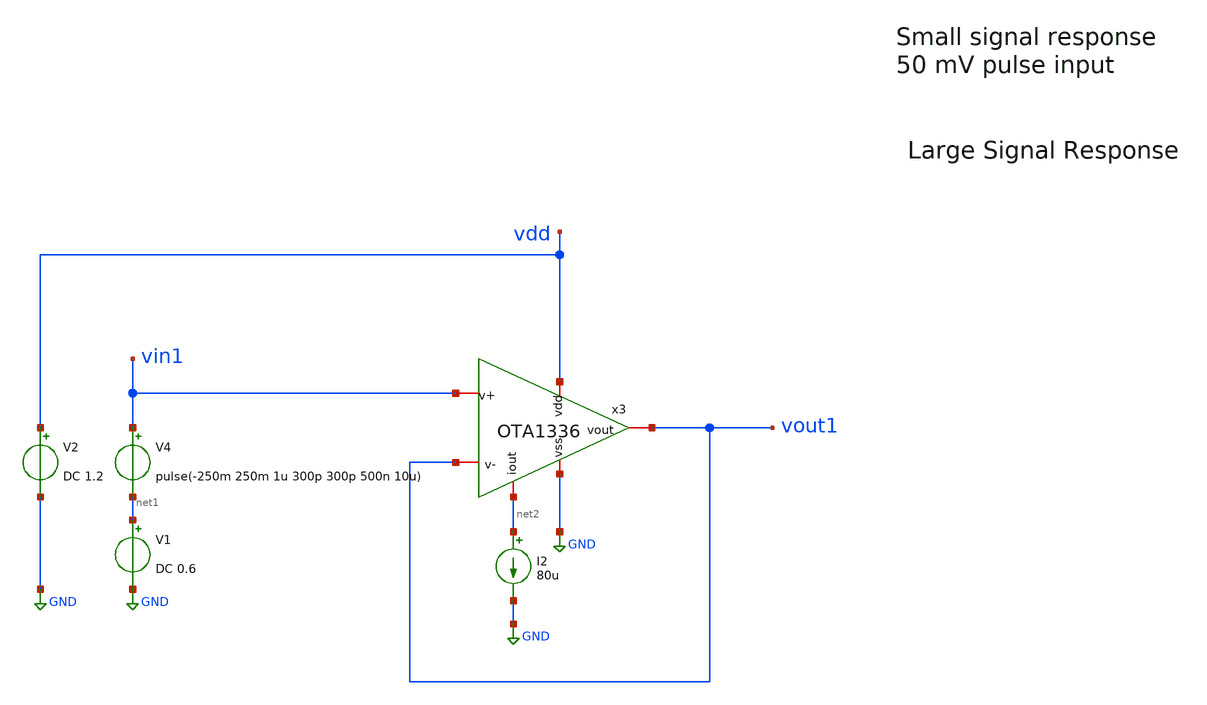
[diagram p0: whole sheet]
** sch_path: tests/data/OTA1336/testbenches/tran/xschem/OTA1336_slew_rate_tb.sch
**.subckt OTA1336_slew_rate_tb
I2 net2 GND 80u
V2 vdd GND DC 1.2
x3 vdd net2 vout1 vout1 vin1 GND OTA1336
V1 net1 GND DC 0.6
V4 vin1 net1 pulse(-250m 250m 1u 300p 300p 500n 10u)
**** begin user architecture code

.lib cornerCAP.lib cap_typ
.lib cornerMOSlv.lib mos_tt
.lib cornerRES.lib res_typ



.control
save all
tran 1n 2u
meas tran Vmax MAX v(vout1) from=750n to=1.5u
let ovshoot = $&vmax/0.65
echo $&ovshoot
write slew_rate.raw

.endc


**** end user architecture code
**.ends
.GLOBAL GND
.end
